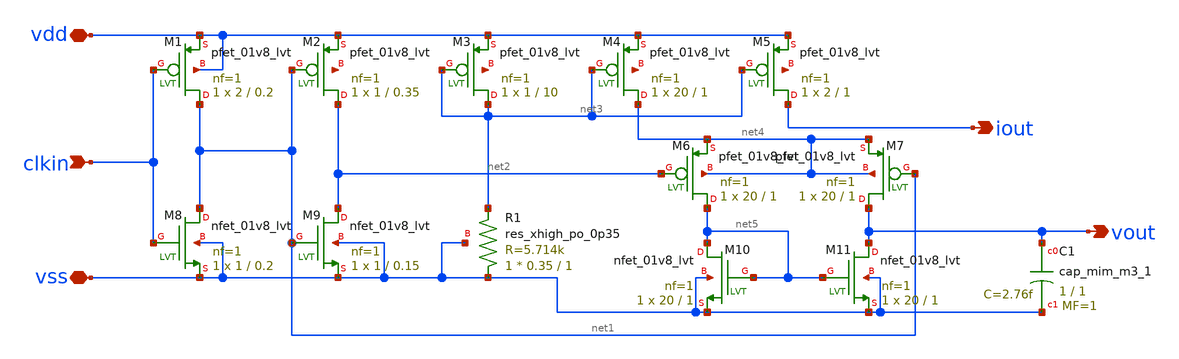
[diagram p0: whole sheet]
** sch_path: Circuits/lowpowersystem1/xschem/CurrentSteeringRampGnerator3sym.sch
**.subckt CurrentSteeringRampGnerator3sym vss vdd clkin iout vout
*.iopin vss
*.iopin vdd
*.ipin clkin
*.opin iout
*.opin vout
XM1 net1 clkin vdd vdd sky130_fd_pr__pfet_01v8_lvt L=0.2 W=2 nf=1 ad='int((nf+1)/2) * W/nf * 0.29' as='int((nf+2)/2) * W/nf * 0.29'
+ pd='2*int((nf+1)/2) * (W/nf + 0.29)' ps='2*int((nf+2)/2) * (W/nf + 0.29)' nrd='0.29 / W' nrs='0.29 / W'
+ sa=0 sb=0 sd=0 mult=1 m=1
XM2 net2 net1 vdd net6 sky130_fd_pr__pfet_01v8_lvt L=0.35 W=1 nf=1 ad='int((nf+1)/2) * W/nf * 0.29' as='int((nf+2)/2) * W/nf * 0.29'
+ pd='2*int((nf+1)/2) * (W/nf + 0.29)' ps='2*int((nf+2)/2) * (W/nf + 0.29)' nrd='0.29 / W' nrs='0.29 / W'
+ sa=0 sb=0 sd=0 mult=1 m=1
XM3 net3 net3 vdd net7 sky130_fd_pr__pfet_01v8_lvt L=10 W=1 nf=1 ad='int((nf+1)/2) * W/nf * 0.29' as='int((nf+2)/2) * W/nf * 0.29'
+ pd='2*int((nf+1)/2) * (W/nf + 0.29)' ps='2*int((nf+2)/2) * (W/nf + 0.29)' nrd='0.29 / W' nrs='0.29 / W'
+ sa=0 sb=0 sd=0 mult=1 m=1
XM4 net4 net3 vdd net8 sky130_fd_pr__pfet_01v8_lvt L=1 W=20 nf=1 ad='int((nf+1)/2) * W/nf * 0.29' as='int((nf+2)/2) * W/nf * 0.29'
+ pd='2*int((nf+1)/2) * (W/nf + 0.29)' ps='2*int((nf+2)/2) * (W/nf + 0.29)' nrd='0.29 / W' nrs='0.29 / W'
+ sa=0 sb=0 sd=0 mult=1 m=1
XM5 iout net3 vdd net9 sky130_fd_pr__pfet_01v8_lvt L=1 W=2 nf=1 ad='int((nf+1)/2) * W/nf * 0.29' as='int((nf+2)/2) * W/nf * 0.29'
+ pd='2*int((nf+1)/2) * (W/nf + 0.29)' ps='2*int((nf+2)/2) * (W/nf + 0.29)' nrd='0.29 / W' nrs='0.29 / W'
+ sa=0 sb=0 sd=0 mult=1 m=1
XM6 net5 net2 net4 net4 sky130_fd_pr__pfet_01v8_lvt L=1 W=20 nf=1 ad='int((nf+1)/2) * W/nf * 0.29' as='int((nf+2)/2) * W/nf * 0.29'
+ pd='2*int((nf+1)/2) * (W/nf + 0.29)' ps='2*int((nf+2)/2) * (W/nf + 0.29)' nrd='0.29 / W' nrs='0.29 / W'
+ sa=0 sb=0 sd=0 mult=1 m=1
XM7 vout net1 net4 net4 sky130_fd_pr__pfet_01v8_lvt L=1 W=20 nf=1 ad='int((nf+1)/2) * W/nf * 0.29' as='int((nf+2)/2) * W/nf * 0.29'
+ pd='2*int((nf+1)/2) * (W/nf + 0.29)' ps='2*int((nf+2)/2) * (W/nf + 0.29)' nrd='0.29 / W' nrs='0.29 / W'
+ sa=0 sb=0 sd=0 mult=1 m=1
XM8 net1 clkin vss vss sky130_fd_pr__nfet_01v8_lvt L=0.2 W=1 nf=1 ad='int((nf+1)/2) * W/nf * 0.29' as='int((nf+2)/2) * W/nf * 0.29'
+ pd='2*int((nf+1)/2) * (W/nf + 0.29)' ps='2*int((nf+2)/2) * (W/nf + 0.29)' nrd='0.29 / W' nrs='0.29 / W'
+ sa=0 sb=0 sd=0 mult=1 m=1
XM9 net2 net1 vss vss sky130_fd_pr__nfet_01v8_lvt L=0.15 W=1 nf=1 ad='int((nf+1)/2) * W/nf * 0.29' as='int((nf+2)/2) * W/nf * 0.29'
+ pd='2*int((nf+1)/2) * (W/nf + 0.29)' ps='2*int((nf+2)/2) * (W/nf + 0.29)' nrd='0.29 / W' nrs='0.29 / W'
+ sa=0 sb=0 sd=0 mult=1 m=1
XM10 net5 net5 vss vss sky130_fd_pr__nfet_01v8_lvt L=1 W=20 nf=1 ad='int((nf+1)/2) * W/nf * 0.29' as='int((nf+2)/2) * W/nf * 0.29'
+ pd='2*int((nf+1)/2) * (W/nf + 0.29)' ps='2*int((nf+2)/2) * (W/nf + 0.29)' nrd='0.29 / W' nrs='0.29 / W'
+ sa=0 sb=0 sd=0 mult=1 m=1
XM11 vout net5 vss vss sky130_fd_pr__nfet_01v8_lvt L=1 W=20 nf=1 ad='int((nf+1)/2) * W/nf * 0.29' as='int((nf+2)/2) * W/nf * 0.29'
+ pd='2*int((nf+1)/2) * (W/nf + 0.29)' ps='2*int((nf+2)/2) * (W/nf + 0.29)' nrd='0.29 / W' nrs='0.29 / W'
+ sa=0 sb=0 sd=0 mult=1 m=1
XR1 vss net3 vss sky130_fd_pr__res_xhigh_po_0p35 L=1 mult=1 m=1
XC1 vout vss sky130_fd_pr__cap_mim_m3_1 W=1 L=1 MF=1 m=1
**.ends
.end
